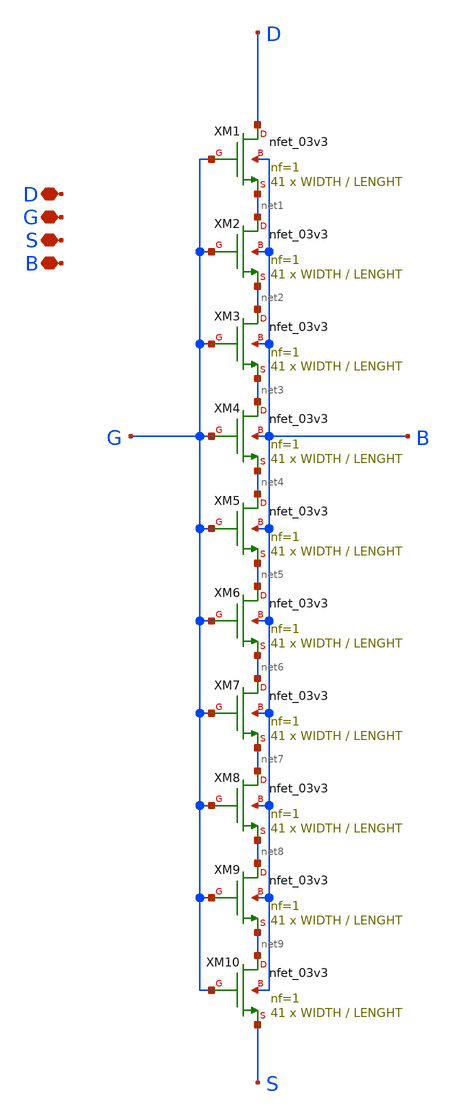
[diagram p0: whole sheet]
** sch_path: New_Extraction/Association/M1_ass.sch
**.subckt M1_ass D G S B
*.iopin D
*.iopin G
*.iopin S
*.iopin B
XM1 D G net1 B nfet_03v3 L=LENGHT W=WIDTH nf=1 ad='int((nf+1)/2) * W/nf * 0.18u' as='int((nf+2)/2) * W/nf * 0.18u'
+ pd='2*int((nf+1)/2) * (W/nf + 0.18u)' ps='2*int((nf+2)/2) * (W/nf + 0.18u)' nrd='0.18u / W' nrs='0.18u / W'
+ sa=0 sb=0 sd=0 m=41
XM2 net1 G net2 B nfet_03v3 L=LENGHT W=WIDTH nf=1 ad='int((nf+1)/2) * W/nf * 0.18u' as='int((nf+2)/2) * W/nf * 0.18u'
+ pd='2*int((nf+1)/2) * (W/nf + 0.18u)' ps='2*int((nf+2)/2) * (W/nf + 0.18u)' nrd='0.18u / W' nrs='0.18u / W'
+ sa=0 sb=0 sd=0 m=41
XM3 net2 G net3 B nfet_03v3 L=LENGHT W=WIDTH nf=1 ad='int((nf+1)/2) * W/nf * 0.18u' as='int((nf+2)/2) * W/nf * 0.18u'
+ pd='2*int((nf+1)/2) * (W/nf + 0.18u)' ps='2*int((nf+2)/2) * (W/nf + 0.18u)' nrd='0.18u / W' nrs='0.18u / W'
+ sa=0 sb=0 sd=0 m=41
XM4 net3 G net4 B nfet_03v3 L=LENGHT W=WIDTH nf=1 ad='int((nf+1)/2) * W/nf * 0.18u' as='int((nf+2)/2) * W/nf * 0.18u'
+ pd='2*int((nf+1)/2) * (W/nf + 0.18u)' ps='2*int((nf+2)/2) * (W/nf + 0.18u)' nrd='0.18u / W' nrs='0.18u / W'
+ sa=0 sb=0 sd=0 m=41
XM5 net4 G net5 B nfet_03v3 L=LENGHT W=WIDTH nf=1 ad='int((nf+1)/2) * W/nf * 0.18u' as='int((nf+2)/2) * W/nf * 0.18u'
+ pd='2*int((nf+1)/2) * (W/nf + 0.18u)' ps='2*int((nf+2)/2) * (W/nf + 0.18u)' nrd='0.18u / W' nrs='0.18u / W'
+ sa=0 sb=0 sd=0 m=41
XM6 net5 G net6 B nfet_03v3 L=LENGHT W=WIDTH nf=1 ad='int((nf+1)/2) * W/nf * 0.18u' as='int((nf+2)/2) * W/nf * 0.18u'
+ pd='2*int((nf+1)/2) * (W/nf + 0.18u)' ps='2*int((nf+2)/2) * (W/nf + 0.18u)' nrd='0.18u / W' nrs='0.18u / W'
+ sa=0 sb=0 sd=0 m=41
XM7 net6 G net7 B nfet_03v3 L=LENGHT W=WIDTH nf=1 ad='int((nf+1)/2) * W/nf * 0.18u' as='int((nf+2)/2) * W/nf * 0.18u'
+ pd='2*int((nf+1)/2) * (W/nf + 0.18u)' ps='2*int((nf+2)/2) * (W/nf + 0.18u)' nrd='0.18u / W' nrs='0.18u / W'
+ sa=0 sb=0 sd=0 m=41
XM8 net7 G net8 B nfet_03v3 L=LENGHT W=WIDTH nf=1 ad='int((nf+1)/2) * W/nf * 0.18u' as='int((nf+2)/2) * W/nf * 0.18u'
+ pd='2*int((nf+1)/2) * (W/nf + 0.18u)' ps='2*int((nf+2)/2) * (W/nf + 0.18u)' nrd='0.18u / W' nrs='0.18u / W'
+ sa=0 sb=0 sd=0 m=41
XM9 net8 G net9 B nfet_03v3 L=LENGHT W=WIDTH nf=1 ad='int((nf+1)/2) * W/nf * 0.18u' as='int((nf+2)/2) * W/nf * 0.18u'
+ pd='2*int((nf+1)/2) * (W/nf + 0.18u)' ps='2*int((nf+2)/2) * (W/nf + 0.18u)' nrd='0.18u / W' nrs='0.18u / W'
+ sa=0 sb=0 sd=0 m=41
XM10 net9 G S B nfet_03v3 L=LENGHT W=WIDTH nf=1 ad='int((nf+1)/2) * W/nf * 0.18u' as='int((nf+2)/2) * W/nf * 0.18u'
+ pd='2*int((nf+1)/2) * (W/nf + 0.18u)' ps='2*int((nf+2)/2) * (W/nf + 0.18u)' nrd='0.18u / W' nrs='0.18u / W'
+ sa=0 sb=0 sd=0 m=41
**.ends
.end
